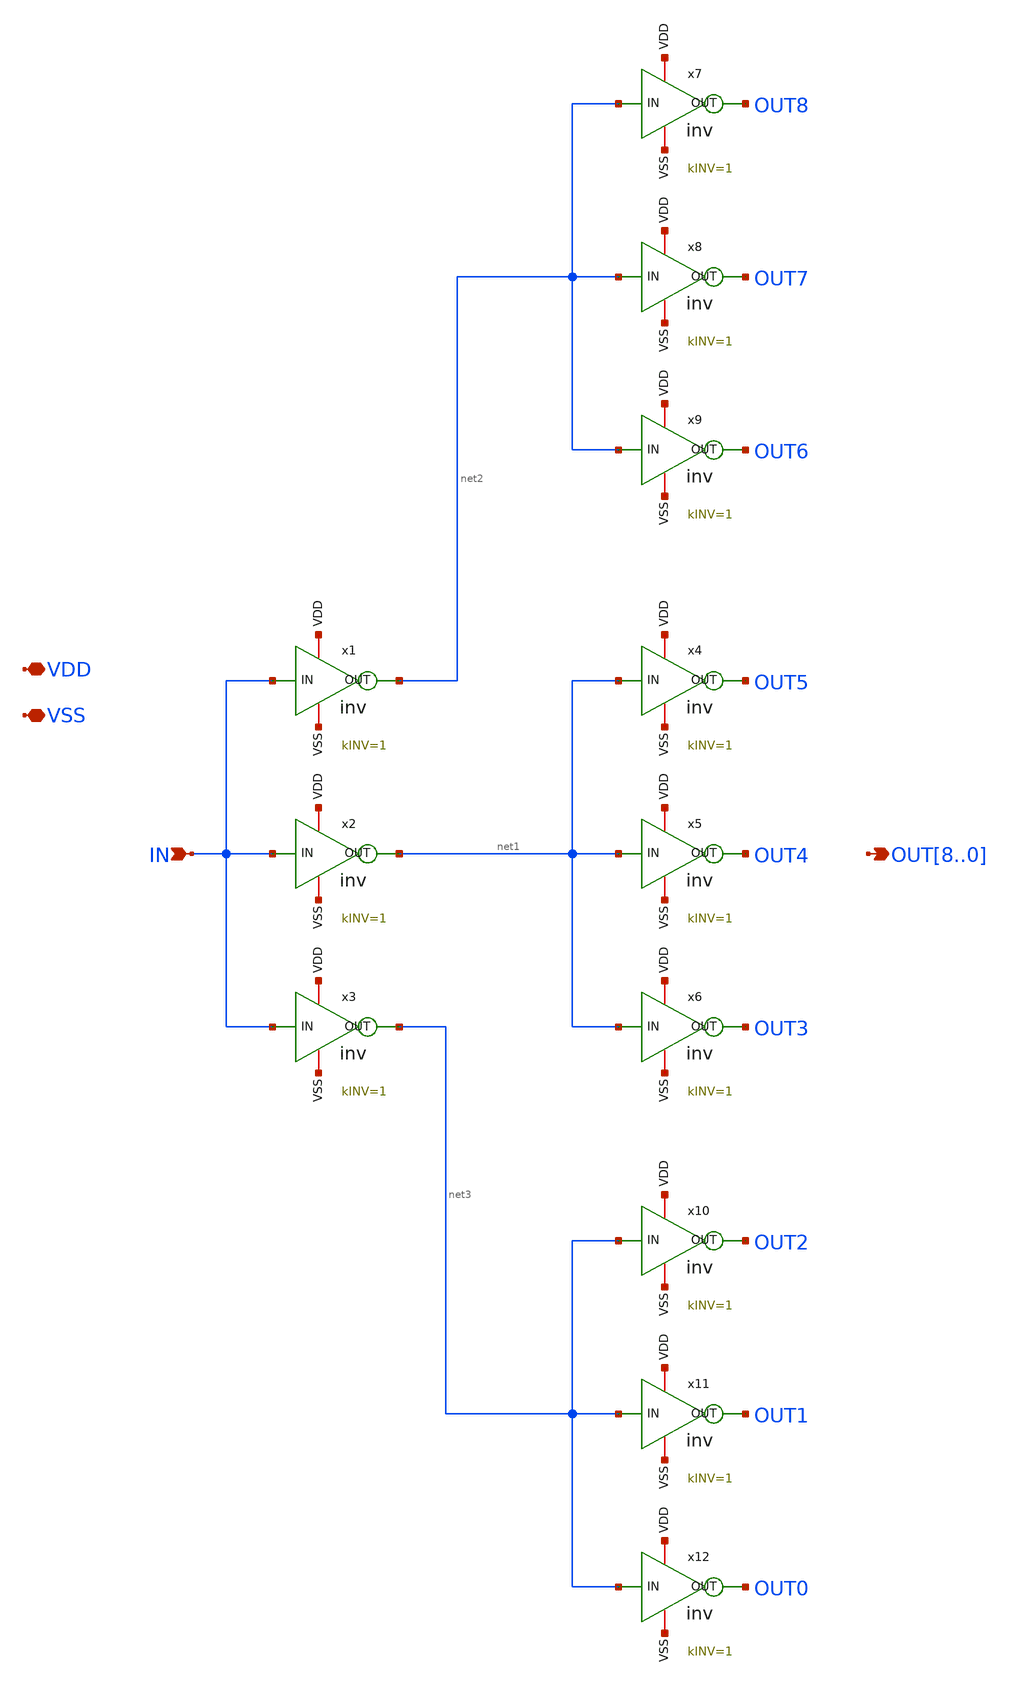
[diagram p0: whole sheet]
** sch_path: CAD6/sign_extend.sch
**.subckt sign_extend IN OUT8,OUT7,OUT6,OUT5,OUT4,OUT3,OUT2,OUT1,OUT0 VDD VSS
*.ipin IN
*.opin OUT8,OUT7,OUT6,OUT5,OUT4,OUT3,OUT2,OUT1,OUT0
*.iopin VDD
*.iopin VSS
x1 net4 IN net2 net5 inv kINV=
x2 net6 IN net1 net7 inv kINV=
x3 net8 IN net3 net9 inv kINV=
x4 net10 net1 OUT5 net11 inv kINV=
x5 net12 net1 OUT4 net13 inv kINV=
x6 net14 net1 OUT3 net15 inv kINV=
x7 net16 net2 OUT8 net17 inv kINV=
x8 net18 net2 OUT7 net19 inv kINV=
x9 net20 net2 OUT6 net21 inv kINV=
x10 net22 net3 OUT2 net23 inv kINV=
x11 net24 net3 OUT1 net25 inv kINV=
x12 net26 net3 OUT0 net27 inv kINV=
**.ends
.end
